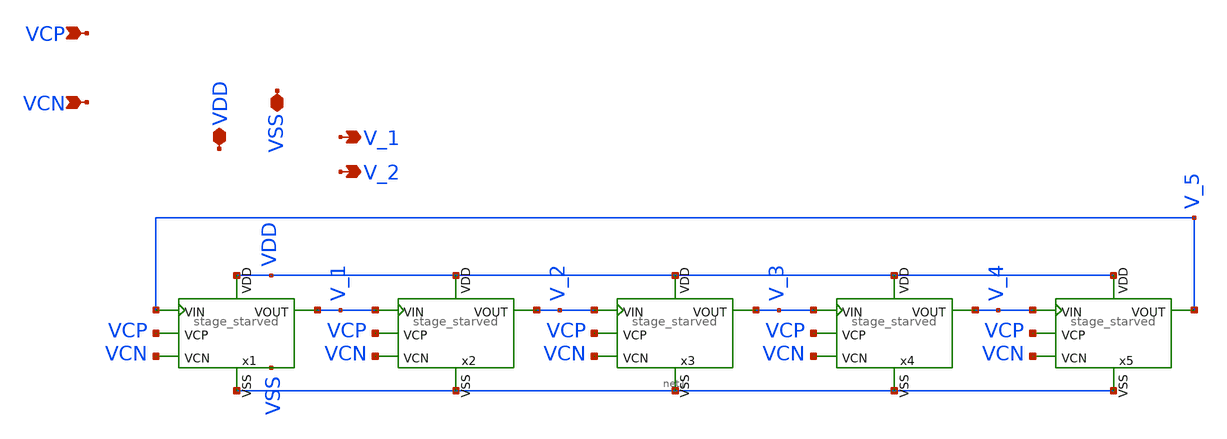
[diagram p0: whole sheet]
** sch_path: xschem/VCO/Starved_VCO.sch
**.subckt Starved_VCO VCP VDD VSS V_1 V_2 VCN
*.ipin VCP
*.iopin VDD
*.iopin VSS
*.opin V_1
*.opin V_2
*.ipin VCN
x1 VDD VCP V_1 V_5 net1 VCN stage_starved
x2 VDD VCP V_2 V_1 net1 VCN stage_starved
x3 VDD VCP V_3 V_2 net1 VCN stage_starved
x4 VDD VCP V_4 V_3 net1 VCN stage_starved
x5 VDD VCP V_5 V_4 net1 VCN stage_starved
**.ends

* expanding   symbol:
*+  /workspaces/usm-vlsi-tools/shared_xserver/simulations/SKY130/IPD500-TimebasedDCDCBuck/VCO/stage_starved.sym # of pins=6
** sym_path: xschem/VCO/stage_starved.sym
** sch_path: xschem/VCO/stage_starved.sch
.subckt stage_starved VDD VCP VOUT VIN VSS VCN
*.ipin VIN
*.opin VOUT
*.iopin VDD
*.iopin VSS
*.ipin VCP
*.ipin VCN
XMP3 net2 VCP VDD VDD sky130_fd_pr__pfet_01v8 L={l_MP3} W={w_MP3} nf=1 ad='int((nf+1)/2) * W/nf * 0.29'
+ as='int((nf+2)/2) * W/nf * 0.29' pd='2*int((nf+1)/2) * (W/nf + 0.29)' ps='2*int((nf+2)/2) * (W/nf + 0.29)'
+ nrd='0.29 / W' nrs='0.29 / W' sa=0 sb=0 sd=0 mult=1 m=1
XMP4 VOUT VIN net3 VDD sky130_fd_pr__pfet_01v8 L={l_MP4} W={w_MP4} nf=1 ad='int((nf+1)/2) * W/nf * 0.29'
+ as='int((nf+2)/2) * W/nf * 0.29' pd='2*int((nf+1)/2) * (W/nf + 0.29)' ps='2*int((nf+2)/2) * (W/nf + 0.29)'
+ nrd='0.29 / W' nrs='0.29 / W' sa=0 sb=0 sd=0 mult=1 m=1
XMN4 VOUT VIN net4 VSS sky130_fd_pr__nfet_01v8 L={l_MN4} W={w_MN4} nf=1 ad='int((nf+1)/2) * W/nf * 0.29'
+ as='int((nf+2)/2) * W/nf * 0.29' pd='2*int((nf+1)/2) * (W/nf + 0.29)' ps='2*int((nf+2)/2) * (W/nf + 0.29)'
+ nrd='0.29 / W' nrs='0.29 / W' sa=0 sb=0 sd=0 mult=1 m=1
VIp net2 net3 0
.save i(vip)
VIn net4 net1 0
.save i(vin)
XMN3 net1 VCN VSS VSS sky130_fd_pr__nfet_01v8 L={l_MN3} W={w_MN3} nf=1 ad='int((nf+1)/2) * W/nf * 0.29'
+ as='int((nf+2)/2) * W/nf * 0.29' pd='2*int((nf+1)/2) * (W/nf + 0.29)' ps='2*int((nf+2)/2) * (W/nf + 0.29)'
+ nrd='0.29 / W' nrs='0.29 / W' sa=0 sb=0 sd=0 mult=1 m=1
.ends

.end
